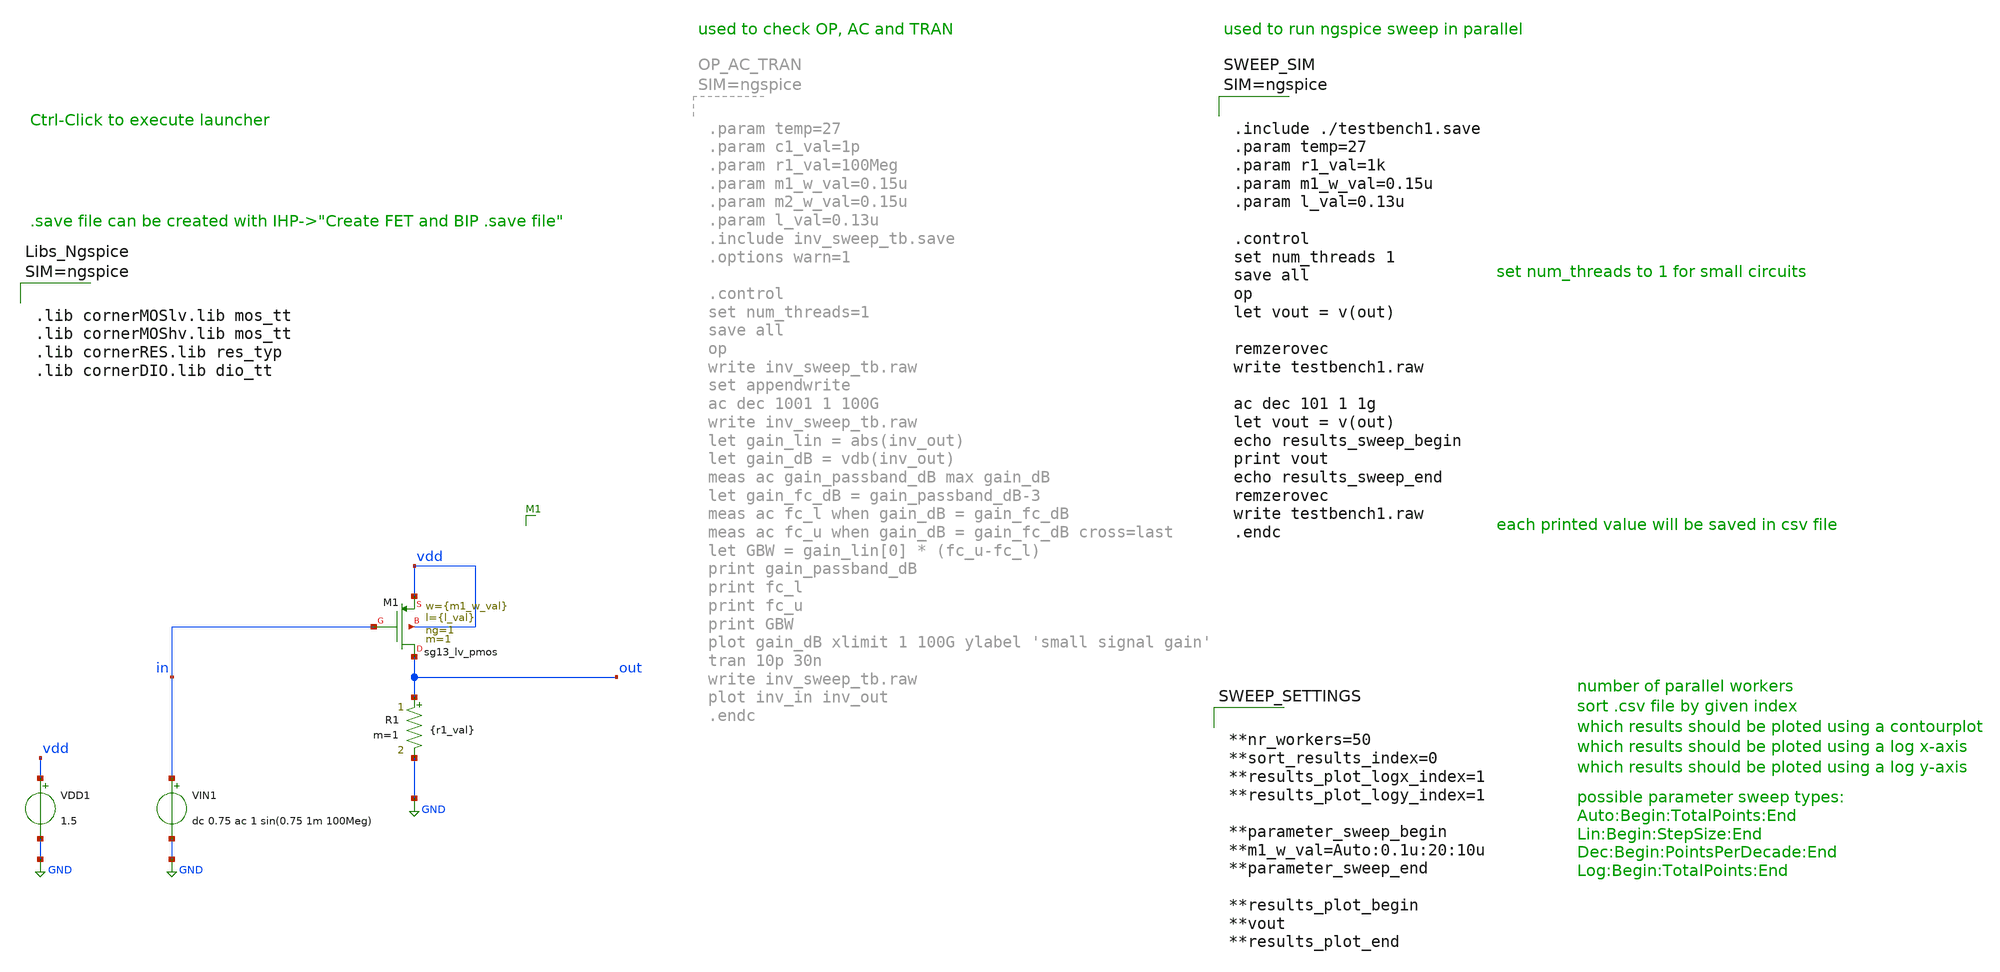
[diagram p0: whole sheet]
** sch_path: macros/filter_cmos5l/testbenches/xschem/testbench1.sch
**.subckt testbench1
VDD1 vdd GND 1.5
XM1 out in vdd vdd sg13_lv_pmos w={m1_w_val} l={l_val} ng=1 m=1 mm_ok=1
VIN1 in GND dc 0.75 ac 1 sin(0.75 1m 100Meg)
R1 out GND {r1_val} m=1
**** begin user architecture code



.include ./testbench1.save
.param temp=27
.param r1_val=1k
.param m1_w_val=0.15u
.param l_val=0.13u

.control
set num_threads 1
save all
op
let vout = v(out)

remzerovec
write testbench1.raw

ac dec 101 1 1g
let vout = v(out)
echo results_sweep_begin
print vout
echo results_sweep_end
remzerovec
write testbench1.raw
.endc





**nr_workers=50
**sort_results_index=0
**results_plot_logx_index=1
**results_plot_logy_index=1

**parameter_sweep_begin
**m1_w_val=Auto:0.1u:20:10u
**parameter_sweep_end

**results_plot_begin
**vout
**results_plot_end





.lib cornerMOSlv.lib mos_tt
.lib cornerMOShv.lib mos_tt
.lib cornerRES.lib res_typ
.lib cornerDIO.lib dio_tt



**** end user architecture code
**.ends
.GLOBAL GND
.end
